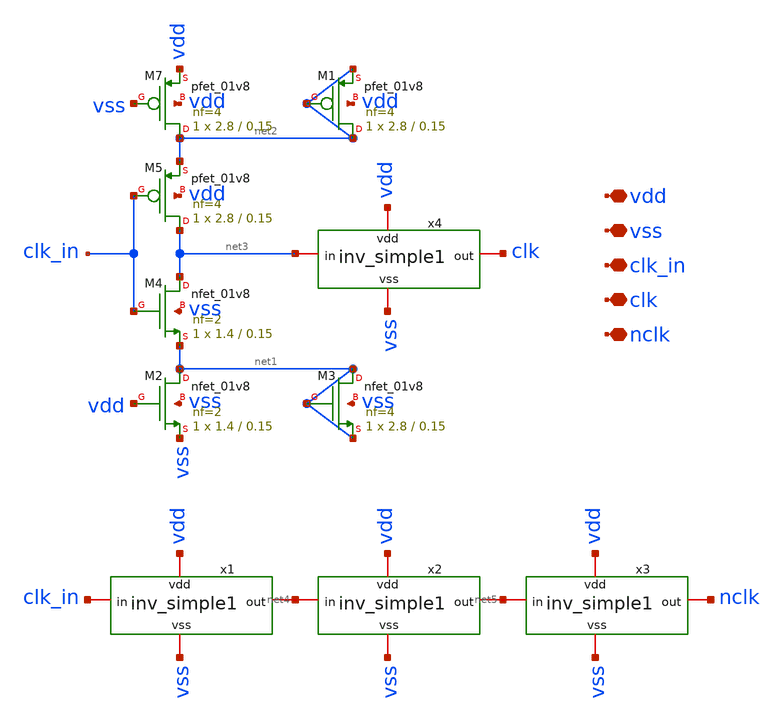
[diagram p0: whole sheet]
** sch_path: xschem/differential.sch
**.subckt differential vdd vss clk_in clk nclk
*.iopin vdd
*.iopin vss
*.iopin clk_in
*.iopin clk
*.iopin nclk
XM2 net1 vdd vss vss sky130_fd_pr__nfet_01v8 L=0.15 W=1.4 nf=2 ad='int((nf+1)/2) * W/nf * 0.29' as='int((nf+2)/2) * W/nf * 0.29'
+ pd='2*int((nf+1)/2) * (W/nf + 0.29)' ps='2*int((nf+2)/2) * (W/nf + 0.29)' nrd='0.29 / W' nrs='0.29 / W'
+ sa=0 sb=0 sd=0 mult=1 m=1
XM7 net2 vss vdd vdd sky130_fd_pr__pfet_01v8 L=0.15 W=2.8 nf=4 ad='int((nf+1)/2) * W/nf * 0.29' as='int((nf+2)/2) * W/nf * 0.29'
+ pd='2*int((nf+1)/2) * (W/nf + 0.29)' ps='2*int((nf+2)/2) * (W/nf + 0.29)' nrd='0.29 / W' nrs='0.29 / W'
+ sa=0 sb=0 sd=0 mult=1 m=1
x1 vdd clk_in net4 vss inv_simple1
x2 vdd net4 net5 vss inv_simple1
x3 vdd net5 nclk vss inv_simple1
x4 vdd net3 clk vss inv_simple1
XM1 net2 net2 net2 vdd sky130_fd_pr__pfet_01v8 L=0.15 W=2.8 nf=4 ad='int((nf+1)/2) * W/nf * 0.29' as='int((nf+2)/2) * W/nf * 0.29'
+ pd='2*int((nf+1)/2) * (W/nf + 0.29)' ps='2*int((nf+2)/2) * (W/nf + 0.29)' nrd='0.29 / W' nrs='0.29 / W'
+ sa=0 sb=0 sd=0 mult=1 m=1
XM3 net1 net1 net1 vss sky130_fd_pr__nfet_01v8 L=0.15 W=2.8 nf=4 ad='int((nf+1)/2) * W/nf * 0.29' as='int((nf+2)/2) * W/nf * 0.29'
+ pd='2*int((nf+1)/2) * (W/nf + 0.29)' ps='2*int((nf+2)/2) * (W/nf + 0.29)' nrd='0.29 / W' nrs='0.29 / W'
+ sa=0 sb=0 sd=0 mult=1 m=1
XM4 net3 clk_in net1 vss sky130_fd_pr__nfet_01v8 L=0.15 W=1.4 nf=2 ad='int((nf+1)/2) * W/nf * 0.29' as='int((nf+2)/2) * W/nf * 0.29'
+ pd='2*int((nf+1)/2) * (W/nf + 0.29)' ps='2*int((nf+2)/2) * (W/nf + 0.29)' nrd='0.29 / W' nrs='0.29 / W'
+ sa=0 sb=0 sd=0 mult=1 m=1
XM5 net3 clk_in net2 vdd sky130_fd_pr__pfet_01v8 L=0.15 W=2.8 nf=4 ad='int((nf+1)/2) * W/nf * 0.29' as='int((nf+2)/2) * W/nf * 0.29'
+ pd='2*int((nf+1)/2) * (W/nf + 0.29)' ps='2*int((nf+2)/2) * (W/nf + 0.29)' nrd='0.29 / W' nrs='0.29 / W'
+ sa=0 sb=0 sd=0 mult=1 m=1
**.ends

* expanding   symbol:  inv_simple1.sym # of pins=4
** sym_path: xschem/inv_simple1.sym
** sch_path: xschem/inv_simple1.sch
.subckt inv_simple1 vdd in out vss
*.iopin in
*.iopin vdd
*.iopin vss
*.iopin out
XM19 out in vss vss sky130_fd_pr__nfet_01v8 L=0.15 W=1.4 nf=1 ad='int((nf+1)/2) * W/nf * 0.29' as='int((nf+2)/2) * W/nf * 0.29'
+ pd='2*int((nf+1)/2) * (W/nf + 0.29)' ps='2*int((nf+2)/2) * (W/nf + 0.29)' nrd='0.29 / W' nrs='0.29 / W'
+ sa=0 sb=0 sd=0 mult=1 m=1
XM20 out in vdd vdd sky130_fd_pr__pfet_01v8 L=0.15 W=2.8 nf=1 ad='int((nf+1)/2) * W/nf * 0.29' as='int((nf+2)/2) * W/nf * 0.29'
+ pd='2*int((nf+1)/2) * (W/nf + 0.29)' ps='2*int((nf+2)/2) * (W/nf + 0.29)' nrd='0.29 / W' nrs='0.29 / W'
+ sa=0 sb=0 sd=0 mult=1 m=1
XM1 vdd vdd vdd vdd sky130_fd_pr__pfet_01v8 L=0.15 W=1.4 nf=1 ad='int((nf+1)/2) * W/nf * 0.29' as='int((nf+2)/2) * W/nf * 0.29'
+ pd='2*int((nf+1)/2) * (W/nf + 0.29)' ps='2*int((nf+2)/2) * (W/nf + 0.29)' nrd='0.29 / W' nrs='0.29 / W'
+ sa=0 sb=0 sd=0 mult=1 m=1
XM2 vss vss vss vss sky130_fd_pr__nfet_01v8 L=0.15 W=1.4 nf=1 ad='int((nf+1)/2) * W/nf * 0.29' as='int((nf+2)/2) * W/nf * 0.29'
+ pd='2*int((nf+1)/2) * (W/nf + 0.29)' ps='2*int((nf+2)/2) * (W/nf + 0.29)' nrd='0.29 / W' nrs='0.29 / W'
+ sa=0 sb=0 sd=0 mult=1 m=1
.ends

.end
